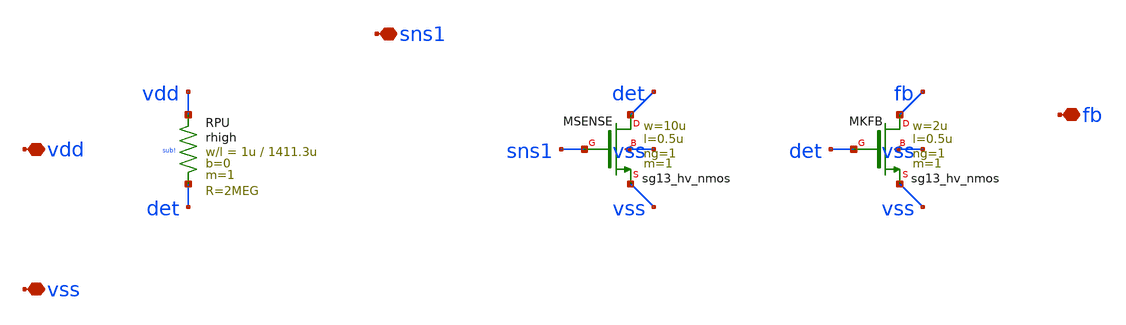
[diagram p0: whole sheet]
** sch_path: designs/g1-guardian/blocks/g1_bgr/source/2AMLogic-sg13g2-bandgap/bandgap_startup.sch
**.subckt bandgap_startup vdd vss sns1 fb
*.iopin vdd
*.iopin vss
*.iopin sns1
*.iopin fb
XRPU vdd det sub! rhigh w=1u l=1411.3u m=1 b=0 mm_ok=1
XMSENSE det sns1 vss vss sg13_hv_nmos w=10u l=0.5u ng=1 m=1 mm_ok=1
XMKFB fb det vss vss sg13_hv_nmos w=2u l=0.5u ng=1 m=1 mm_ok=1
**.ends
.end
